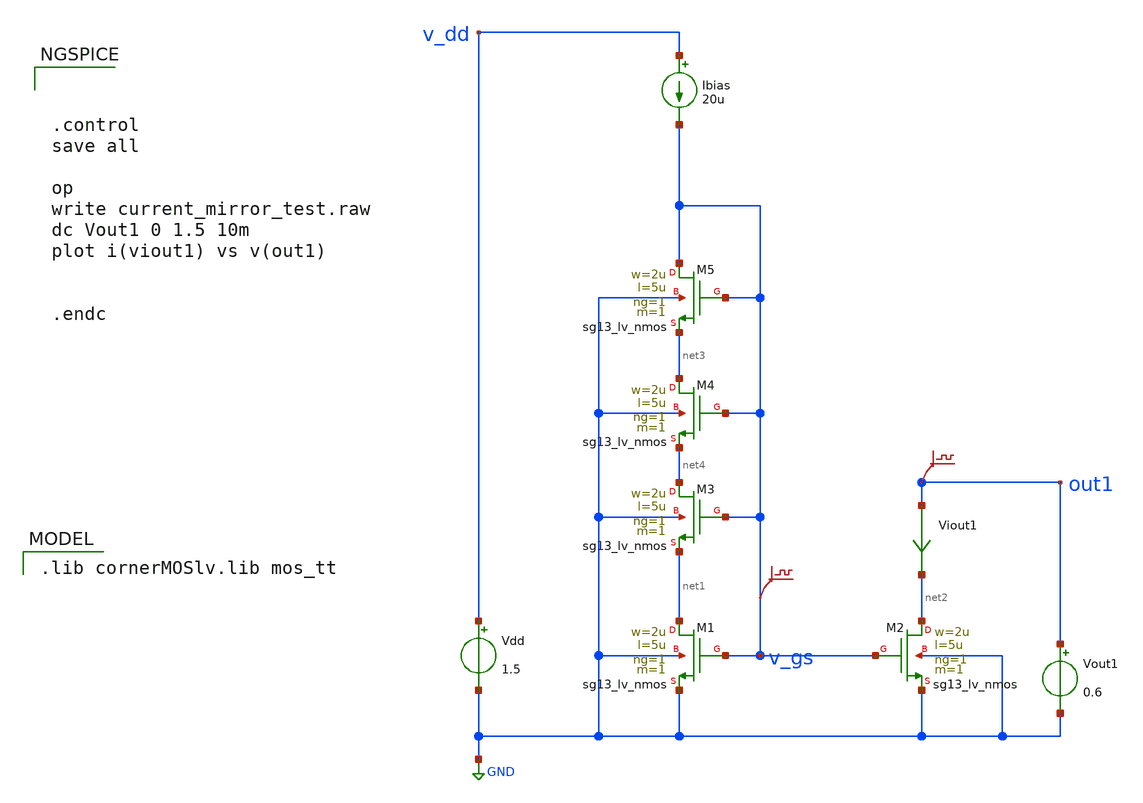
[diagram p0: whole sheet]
** sch_path: Designs/current_mirror/test.sch
* (c) 2025 Thesis_HP, Apache-2.0 license
**.subckt test
Vdd v_dd GND 1.5
XM1 net1 v_gs GND GND sg13_lv_nmos w=2u l=5u ng=1 m=1 mm_ok=1
Ibias v_dd v_gs 20u
XM2 net2 v_gs GND GND sg13_lv_nmos w=2u l=5u ng=1 m=1 mm_ok=1
Vout1 out1 GND 0.6
.save v(out1)
.save v(v_gs)
Viout1 out1 net2 0
.save i(viout1)
XM3 net4 v_gs net1 GND sg13_lv_nmos w=2u l=5u ng=1 m=1 mm_ok=1
XM4 net3 v_gs net4 GND sg13_lv_nmos w=2u l=5u ng=1 m=1 mm_ok=1
XM5 v_gs v_gs net3 GND sg13_lv_nmos w=2u l=5u ng=1 m=1 mm_ok=1
**** begin user architecture code



.control
save all

op
write current_mirror_test.raw
dc Vout1 0 1.5 10m
plot i(viout1) vs v(out1)


.endc


 .lib cornerMOSlv.lib mos_tt

**** end user architecture code
**.ends
.GLOBAL GND
.end
